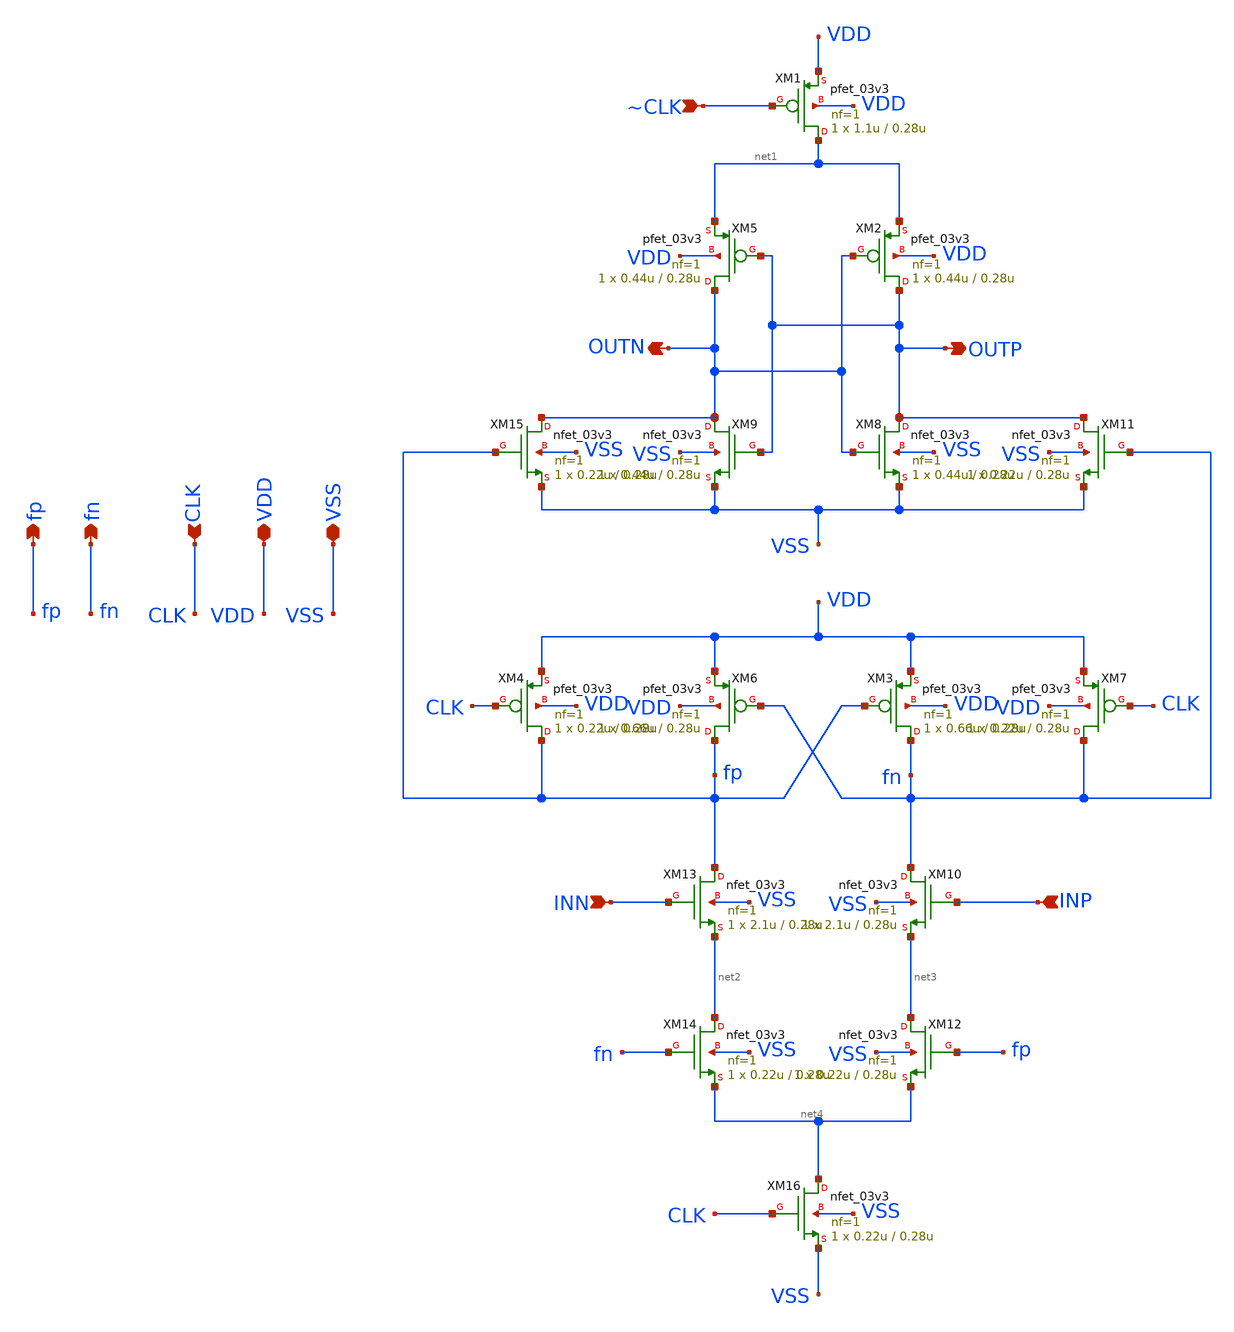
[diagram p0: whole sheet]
** sch_path: analog/blocks/Double_Tail_Comparator/realcomp.sch
**.subckt realcomp INN INP CLK VSS VDD OUTP OUTN ~CLK fn fp
*.ipin INN
*.ipin INP
*.ipin CLK
*.iopin VSS
*.iopin VDD
*.opin OUTP
*.opin OUTN
*.ipin ~CLK
*.opin fn
*.opin fp
XM1 net1 ~CLK VDD VDD pfet_03v3 L=0.28u W=1.1u nf=1 ad='int((nf+1)/2) * W/nf * 0.18u' as='int((nf+2)/2) * W/nf * 0.18u'
+ pd='2*int((nf+1)/2) * (W/nf + 0.18u)' ps='2*int((nf+2)/2) * (W/nf + 0.18u)' nrd='0.18u / W' nrs='0.18u / W'
+ sa=0 sb=0 sd=0 m=1
XM2 OUTP OUTN net1 VDD pfet_03v3 L=0.28u W=0.44u nf=1 ad='int((nf+1)/2) * W/nf * 0.18u' as='int((nf+2)/2) * W/nf * 0.18u'
+ pd='2*int((nf+1)/2) * (W/nf + 0.18u)' ps='2*int((nf+2)/2) * (W/nf + 0.18u)' nrd='0.18u / W' nrs='0.18u / W'
+ sa=0 sb=0 sd=0 m=1
XM3 fn fp VDD VDD pfet_03v3 L=0.28u W=0.66u nf=1 ad='int((nf+1)/2) * W/nf * 0.18u' as='int((nf+2)/2) * W/nf * 0.18u'
+ pd='2*int((nf+1)/2) * (W/nf + 0.18u)' ps='2*int((nf+2)/2) * (W/nf + 0.18u)' nrd='0.18u / W' nrs='0.18u / W'
+ sa=0 sb=0 sd=0 m=1
XM4 fp CLK VDD VDD pfet_03v3 L=0.28u W=0.22u nf=1 ad='int((nf+1)/2) * W/nf * 0.18u' as='int((nf+2)/2) * W/nf * 0.18u'
+ pd='2*int((nf+1)/2) * (W/nf + 0.18u)' ps='2*int((nf+2)/2) * (W/nf + 0.18u)' nrd='0.18u / W' nrs='0.18u / W'
+ sa=0 sb=0 sd=0 m=1
XM5 OUTN OUTP net1 VDD pfet_03v3 L=0.28u W=0.44u nf=1 ad='int((nf+1)/2) * W/nf * 0.18u' as='int((nf+2)/2) * W/nf * 0.18u'
+ pd='2*int((nf+1)/2) * (W/nf + 0.18u)' ps='2*int((nf+2)/2) * (W/nf + 0.18u)' nrd='0.18u / W' nrs='0.18u / W'
+ sa=0 sb=0 sd=0 m=1
XM8 OUTP OUTN VSS VSS nfet_03v3 L=0.28u W=0.44u nf=1 ad='int((nf+1)/2) * W/nf * 0.18u' as='int((nf+2)/2) * W/nf * 0.18u'
+ pd='2*int((nf+1)/2) * (W/nf + 0.18u)' ps='2*int((nf+2)/2) * (W/nf + 0.18u)' nrd='0.18u / W' nrs='0.18u / W'
+ sa=0 sb=0 sd=0 m=1
XM15 OUTN fp VSS VSS nfet_03v3 L=0.28u W=0.22u nf=1 ad='int((nf+1)/2) * W/nf * 0.18u' as='int((nf+2)/2) * W/nf * 0.18u'
+ pd='2*int((nf+1)/2) * (W/nf + 0.18u)' ps='2*int((nf+2)/2) * (W/nf + 0.18u)' nrd='0.18u / W' nrs='0.18u / W'
+ sa=0 sb=0 sd=0 m=1
XM11 OUTP fn VSS VSS nfet_03v3 L=0.28u W=0.22u nf=1 ad='int((nf+1)/2) * W/nf * 0.18u' as='int((nf+2)/2) * W/nf * 0.18u'
+ pd='2*int((nf+1)/2) * (W/nf + 0.18u)' ps='2*int((nf+2)/2) * (W/nf + 0.18u)' nrd='0.18u / W' nrs='0.18u / W'
+ sa=0 sb=0 sd=0 m=1
XM13 fp INN net2 VSS nfet_03v3 L=0.28u W=2.1u nf=1 ad='int((nf+1)/2) * W/nf * 0.18u' as='int((nf+2)/2) * W/nf * 0.18u'
+ pd='2*int((nf+1)/2) * (W/nf + 0.18u)' ps='2*int((nf+2)/2) * (W/nf + 0.18u)' nrd='0.18u / W' nrs='0.18u / W'
+ sa=0 sb=0 sd=0 m=1
XM14 net2 fn net4 VSS nfet_03v3 L=0.28u W=0.22u nf=1 ad='int((nf+1)/2) * W/nf * 0.18u' as='int((nf+2)/2) * W/nf * 0.18u'
+ pd='2*int((nf+1)/2) * (W/nf + 0.18u)' ps='2*int((nf+2)/2) * (W/nf + 0.18u)' nrd='0.18u / W' nrs='0.18u / W'
+ sa=0 sb=0 sd=0 m=1
XM16 net4 CLK VSS VSS nfet_03v3 L=0.28u W=0.22u nf=1 ad='int((nf+1)/2) * W/nf * 0.18u' as='int((nf+2)/2) * W/nf * 0.18u'
+ pd='2*int((nf+1)/2) * (W/nf + 0.18u)' ps='2*int((nf+2)/2) * (W/nf + 0.18u)' nrd='0.18u / W' nrs='0.18u / W'
+ sa=0 sb=0 sd=0 m=1
XM9 OUTN OUTP VSS VSS nfet_03v3 L=0.28u W=0.44u nf=1 ad='int((nf+1)/2) * W/nf * 0.18u' as='int((nf+2)/2) * W/nf * 0.18u'
+ pd='2*int((nf+1)/2) * (W/nf + 0.18u)' ps='2*int((nf+2)/2) * (W/nf + 0.18u)' nrd='0.18u / W' nrs='0.18u / W'
+ sa=0 sb=0 sd=0 m=1
XM6 fp fn VDD VDD pfet_03v3 L=0.28u W=0.66u nf=1 ad='int((nf+1)/2) * W/nf * 0.18u' as='int((nf+2)/2) * W/nf * 0.18u'
+ pd='2*int((nf+1)/2) * (W/nf + 0.18u)' ps='2*int((nf+2)/2) * (W/nf + 0.18u)' nrd='0.18u / W' nrs='0.18u / W'
+ sa=0 sb=0 sd=0 m=1
XM7 fn CLK VDD VDD pfet_03v3 L=0.28u W=0.22u nf=1 ad='int((nf+1)/2) * W/nf * 0.18u' as='int((nf+2)/2) * W/nf * 0.18u'
+ pd='2*int((nf+1)/2) * (W/nf + 0.18u)' ps='2*int((nf+2)/2) * (W/nf + 0.18u)' nrd='0.18u / W' nrs='0.18u / W'
+ sa=0 sb=0 sd=0 m=1
XM10 fn INP net3 VSS nfet_03v3 L=0.28u W=2.1u nf=1 ad='int((nf+1)/2) * W/nf * 0.18u' as='int((nf+2)/2) * W/nf * 0.18u'
+ pd='2*int((nf+1)/2) * (W/nf + 0.18u)' ps='2*int((nf+2)/2) * (W/nf + 0.18u)' nrd='0.18u / W' nrs='0.18u / W'
+ sa=0 sb=0 sd=0 m=1
XM12 net3 fp net4 VSS nfet_03v3 L=0.28u W=0.22u nf=1 ad='int((nf+1)/2) * W/nf * 0.18u' as='int((nf+2)/2) * W/nf * 0.18u'
+ pd='2*int((nf+1)/2) * (W/nf + 0.18u)' ps='2*int((nf+2)/2) * (W/nf + 0.18u)' nrd='0.18u / W' nrs='0.18u / W'
+ sa=0 sb=0 sd=0 m=1
**.ends
.end
